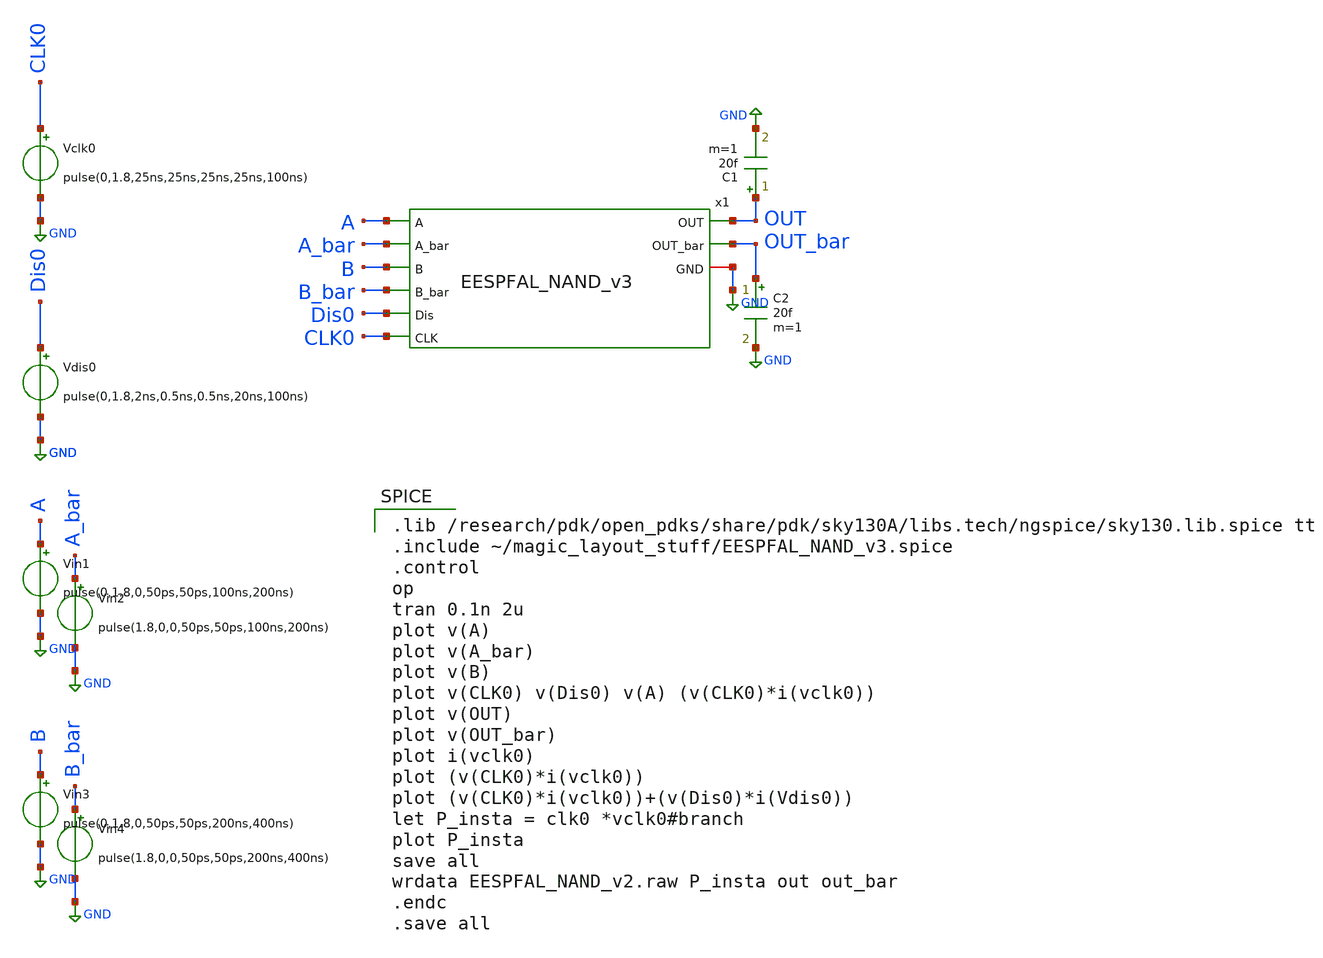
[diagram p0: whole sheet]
** sch_path: skywater_stuff/EESPFAL_NAND_sim.sch
**.subckt EESPFAL_NAND_sim
x1 A A_bar B B_bar OUT OUT_bar Dis0 GND CLK0 EESPFAL_NAND_v3
Vin1 A GND pulse(0,1.8,0,50ps,50ps,100ns,200ns)
Vin2 A_bar GND pulse(1.8,0,0,50ps,50ps,100ns,200ns)
Vdis0 Dis0 GND pulse(0,1.8,2ns,0.5ns,0.5ns,20ns,100ns)
Vin3 B GND pulse(0,1.8,0,50ps,50ps,200ns,400ns)
Vin4 B_bar GND pulse(1.8,0,0,50ps,50ps,200ns,400ns)
C1 OUT GND 20f m=1
C2 OUT_bar GND 20f m=1
Vclk0 CLK0 GND pulse(0,1.8,25ns,25ns,25ns,25ns,100ns)
**** begin user architecture code

.lib /research/pdk/open_pdks/share/pdk/sky130A/libs.tech/ngspice/sky130.lib.spice tt
.include ~/magic_layout_stuff/EESPFAL_NAND_v3.spice
.control
op
tran 0.1n 2u
plot v(A)
plot v(A_bar)
plot v(B)
plot v(CLK0) v(Dis0) v(A) (v(CLK0)*i(vclk0))
plot v(OUT)
plot v(OUT_bar)
plot i(vclk0)
plot (v(CLK0)*i(vclk0))
plot (v(CLK0)*i(vclk0))+(v(Dis0)*i(Vdis0))
let P_insta = clk0 *vclk0#branch
plot P_insta
save all
wrdata EESPFAL_NAND_v2.raw P_insta out out_bar
.endc
.save all


**** end user architecture code
**.ends
.GLOBAL GND
.end
